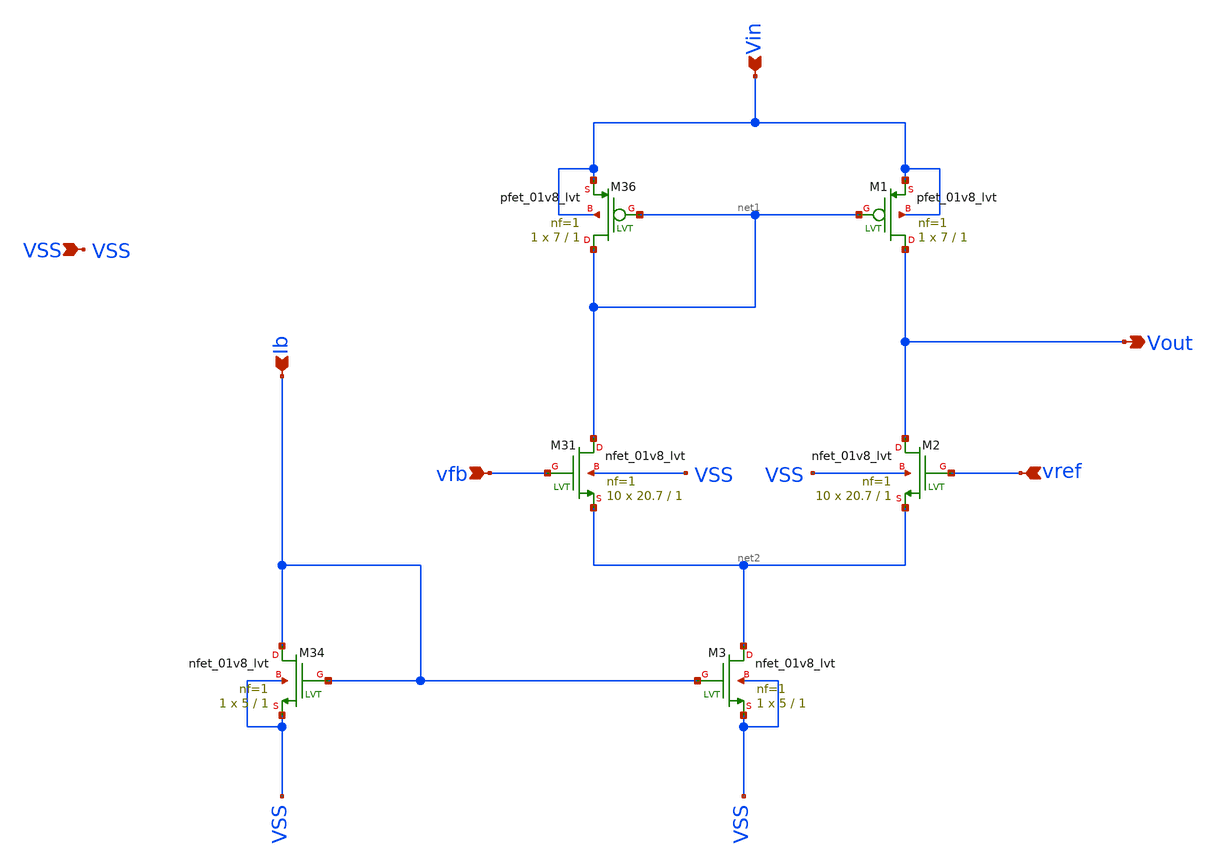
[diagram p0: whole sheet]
** sch_path: Schematics/Err_amp_50u.sch
**.subckt Err_amp_50u Vin VSS Ib Vout vfb vref
*.ipin Vin
*.ipin VSS
*.ipin Ib
*.opin Vout
*.ipin vfb
*.ipin vref
XM36 net1 net1 Vin Vin sky130_fd_pr__pfet_01v8_lvt L=1 W=7 nf=1 ad='int((nf+1)/2) * W/nf * 0.29' as='int((nf+2)/2) * W/nf * 0.29'
+ pd='2*int((nf+1)/2) * (W/nf + 0.29)' ps='2*int((nf+2)/2) * (W/nf + 0.29)' nrd='0.29 / W' nrs='0.29 / W'
+ sa=0 sb=0 sd=0 mult=1 m=1
XM1 Vout net1 Vin Vin sky130_fd_pr__pfet_01v8_lvt L=1 W=7 nf=1 ad='int((nf+1)/2) * W/nf * 0.29' as='int((nf+2)/2) * W/nf * 0.29'
+ pd='2*int((nf+1)/2) * (W/nf + 0.29)' ps='2*int((nf+2)/2) * (W/nf + 0.29)' nrd='0.29 / W' nrs='0.29 / W'
+ sa=0 sb=0 sd=0 mult=1 m=1
XM31 net1 vfb net2 VSS sky130_fd_pr__nfet_01v8_lvt L=1 W=20.7 nf=1 ad='int((nf+1)/2) * W/nf * 0.29' as='int((nf+2)/2) * W/nf * 0.29'
+ pd='2*int((nf+1)/2) * (W/nf + 0.29)' ps='2*int((nf+2)/2) * (W/nf + 0.29)' nrd='0.29 / W' nrs='0.29 / W'
+ sa=0 sb=0 sd=0 mult=10 m=10
XM2 Vout vref net2 VSS sky130_fd_pr__nfet_01v8_lvt L=1 W=20.7 nf=1 ad='int((nf+1)/2) * W/nf * 0.29' as='int((nf+2)/2) * W/nf * 0.29'
+ pd='2*int((nf+1)/2) * (W/nf + 0.29)' ps='2*int((nf+2)/2) * (W/nf + 0.29)' nrd='0.29 / W' nrs='0.29 / W'
+ sa=0 sb=0 sd=0 mult=10 m=10
XM34 Ib Ib VSS VSS sky130_fd_pr__nfet_01v8_lvt L=1 W=5 nf=1 ad='int((nf+1)/2) * W/nf * 0.29' as='int((nf+2)/2) * W/nf * 0.29'
+ pd='2*int((nf+1)/2) * (W/nf + 0.29)' ps='2*int((nf+2)/2) * (W/nf + 0.29)' nrd='0.29 / W' nrs='0.29 / W'
+ sa=0 sb=0 sd=0 mult=1 m=1
XM3 net2 Ib VSS VSS sky130_fd_pr__nfet_01v8_lvt L=1 W=5 nf=1 ad='int((nf+1)/2) * W/nf * 0.29' as='int((nf+2)/2) * W/nf * 0.29'
+ pd='2*int((nf+1)/2) * (W/nf + 0.29)' ps='2*int((nf+2)/2) * (W/nf + 0.29)' nrd='0.29 / W' nrs='0.29 / W'
+ sa=0 sb=0 sd=0 mult=1 m=1
**.ends
.end
